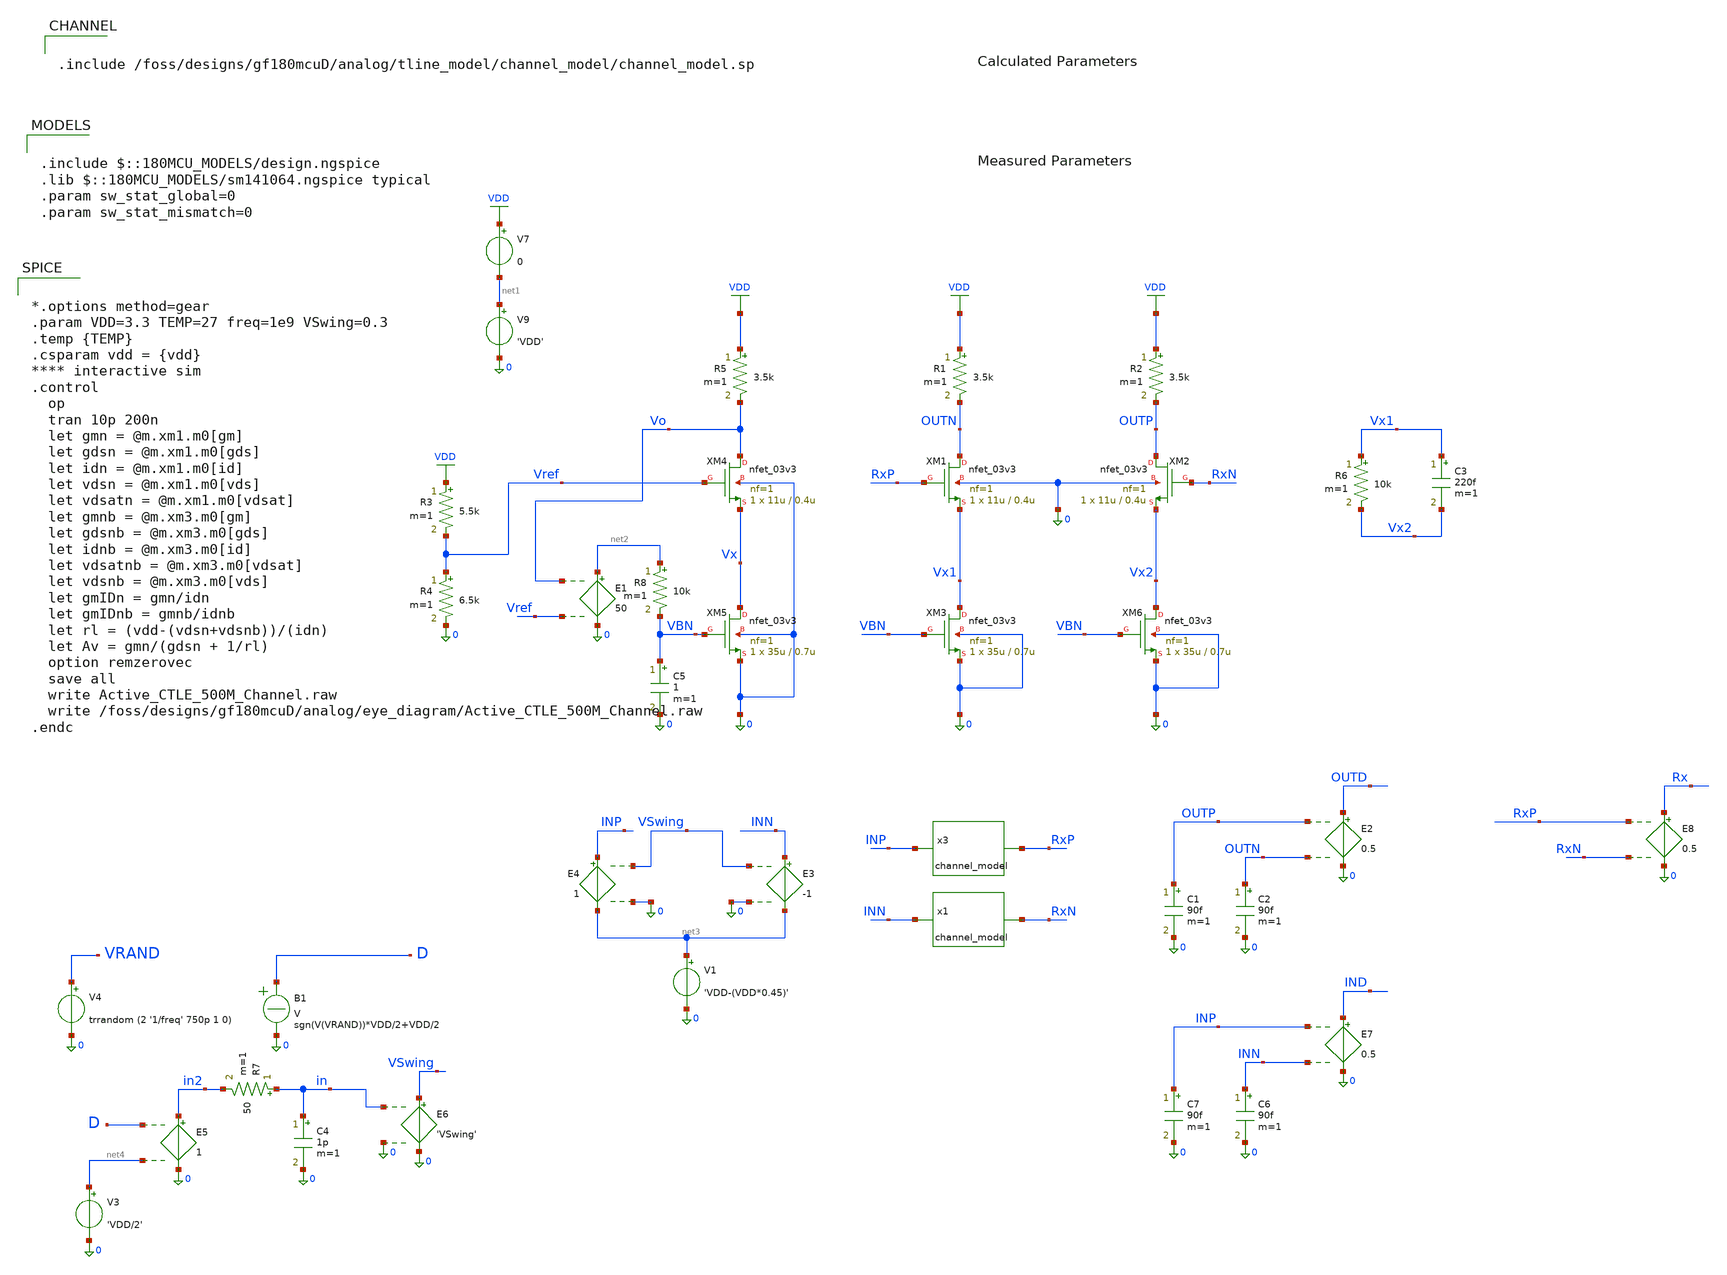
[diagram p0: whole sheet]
** sch_path: Xschem/gf180mcuD/gmID_Designs/Active_CTLE_500M_Channel.sch
**.subckt Active_CTLE_500M_Channel
XM1 OUTN RxP Vx1 0 nfet_03v3 L=0.4u W=11u nf=1 ad='int((nf+1)/2) * W/nf * 0.18u' as='int((nf+2)/2) * W/nf * 0.18u'
+ pd='2*int((nf+1)/2) * (W/nf + 0.18u)' ps='2*int((nf+2)/2) * (W/nf + 0.18u)' nrd='0.18u / W' nrs='0.18u / W'
+ sa=0 sb=0 sd=0 m=1
E1 net2 0 Vo Vref 50
V9 net1 0 'VDD'
V7 VDD net1 0
C2 OUTN 0 90f m=1
XM2 OUTP RxN Vx2 0 nfet_03v3 L=0.4u W=11u nf=1 ad='int((nf+1)/2) * W/nf * 0.18u' as='int((nf+2)/2) * W/nf * 0.18u'
+ pd='2*int((nf+1)/2) * (W/nf + 0.18u)' ps='2*int((nf+2)/2) * (W/nf + 0.18u)' nrd='0.18u / W' nrs='0.18u / W'
+ sa=0 sb=0 sd=0 m=1
R1 VDD OUTN 3.5k m=1
R2 VDD OUTP 3.5k m=1
XM3 Vx1 VBN 0 0 nfet_03v3 L=0.7u W=35u nf=1 ad='int((nf+1)/2) * W/nf * 0.18u' as='int((nf+2)/2) * W/nf * 0.18u'
+ pd='2*int((nf+1)/2) * (W/nf + 0.18u)' ps='2*int((nf+2)/2) * (W/nf + 0.18u)' nrd='0.18u / W' nrs='0.18u / W'
+ sa=0 sb=0 sd=0 m=1
E2 OUTD 0 OUTP OUTN 0.5
C1 OUTP 0 90f m=1
R3 VDD Vref 5.5k m=1
R4 Vref 0 6.5k m=1
XM4 Vo Vref Vx 0 nfet_03v3 L=0.4u W=11u nf=1 ad='int((nf+1)/2) * W/nf * 0.18u' as='int((nf+2)/2) * W/nf * 0.18u'
+ pd='2*int((nf+1)/2) * (W/nf + 0.18u)' ps='2*int((nf+2)/2) * (W/nf + 0.18u)' nrd='0.18u / W' nrs='0.18u / W'
+ sa=0 sb=0 sd=0 m=1
XM5 Vx VBN 0 0 nfet_03v3 L=0.7u W=35u nf=1 ad='int((nf+1)/2) * W/nf * 0.18u' as='int((nf+2)/2) * W/nf * 0.18u'
+ pd='2*int((nf+1)/2) * (W/nf + 0.18u)' ps='2*int((nf+2)/2) * (W/nf + 0.18u)' nrd='0.18u / W' nrs='0.18u / W'
+ sa=0 sb=0 sd=0 m=1
R5 VDD Vo 3.5k m=1
E3 INN net3 VSwing 0 -1
V1 net3 0 'VDD-(VDD*0.45)'
E4 INP net3 VSwing 0 1
XM6 Vx2 VBN 0 0 nfet_03v3 L=0.7u W=35u nf=1 ad='int((nf+1)/2) * W/nf * 0.18u' as='int((nf+2)/2) * W/nf * 0.18u'
+ pd='2*int((nf+1)/2) * (W/nf + 0.18u)' ps='2*int((nf+2)/2) * (W/nf + 0.18u)' nrd='0.18u / W' nrs='0.18u / W'
+ sa=0 sb=0 sd=0 m=1
R6 Vx1 Vx2 10k m=1
C3 Vx1 Vx2 220f m=1
V4 VRAND 0 trrandom (2 '1/freq' 750p 1 0)
B1 D 0 V = sgn(V(VRAND))*VDD/2+VDD/2
E5 in2 0 D net4 1
R7 in in2 50 m=1
C4 in 0 1p m=1
V3 net4 0 'VDD/2'
E6 VSwing 0 in 0 'VSwing'
R8 net2 VBN 10k m=1
C5 VBN 0 1 m=1
C6 INN 0 90f m=1
E7 IND 0 INP INN 0.5
C7 INP 0 90f m=1
E8 Rx 0 RxP RxN 0.5
x3 INP RxP channel_model
x1 INN RxN channel_model
**** begin user architecture code

.include $::180MCU_MODELS/design.ngspice
.lib $::180MCU_MODELS/sm141064.ngspice typical
.param sw_stat_global=0
.param sw_stat_mismatch=0



*.options method=gear
.param VDD=3.3 TEMP=27 freq=1e9 VSwing=0.3
.temp {TEMP}
.csparam vdd = {vdd}
**** interactive sim
.control
  op
  tran 10p 200n
  let gmn = @m.xm1.m0[gm]
  let gdsn = @m.xm1.m0[gds]
  let idn = @m.xm1.m0[id]
  let vdsn = @m.xm1.m0[vds]
  let vdsatn = @m.xm1.m0[vdsat]
  let gmnb = @m.xm3.m0[gm]
  let gdsnb = @m.xm3.m0[gds]
  let idnb = @m.xm3.m0[id]
  let vdsatnb = @m.xm3.m0[vdsat]
  let vdsnb = @m.xm3.m0[vds]
  let gmIDn = gmn/idn
  let gmIDnb = gmnb/idnb
  let rl = (vdd-(vdsn+vdsnb))/(idn)
  let Av = gmn/(gdsn + 1/rl)
  option remzerovec
  save all
  write Active_CTLE_500M_Channel.raw
  write /foss/designs/gf180mcuD/analog/eye_diagram/Active_CTLE_500M_Channel.raw
.endc



.include /foss/designs/gf180mcuD/analog/tline_model/channel_model/channel_model.sp
**** end user architecture code
**.ends
.GLOBAL VDD
.end
